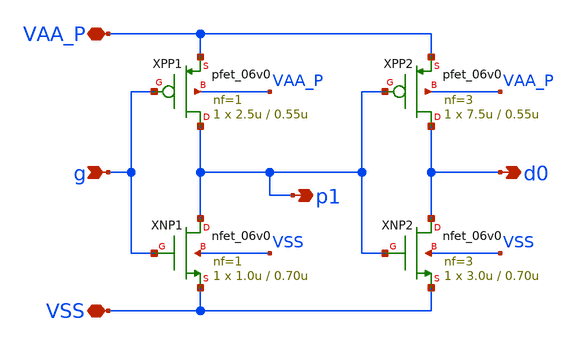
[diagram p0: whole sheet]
** sch_path: xschem/ck_p.sch
**.subckt ck_p g VAA_P d0 p1 VSS
*.ipin g
*.iopin VAA_P
*.opin d0
*.opin p1
*.iopin VSS
XPP1 p1 g VAA_P VAA_P pfet_06v0 L=0.55u W=2.5u nf=1 ad='int((nf+1)/2) * W/nf * 0.18u' as='int((nf+2)/2) * W/nf * 0.18u'
+ pd='2*int((nf+1)/2) * (W/nf + 0.18u)' ps='2*int((nf+2)/2) * (W/nf + 0.18u)' nrd='0.18u / W' nrs='0.18u / W'
+ sa=0 sb=0 sd=0 m=1
XPP2 d0 p1 VAA_P VAA_P pfet_06v0 L=0.55u W=7.5u nf=3 ad='int((nf+1)/2) * W/nf * 0.18u' as='int((nf+2)/2) * W/nf * 0.18u'
+ pd='2*int((nf+1)/2) * (W/nf + 0.18u)' ps='2*int((nf+2)/2) * (W/nf + 0.18u)' nrd='0.18u / W' nrs='0.18u / W'
+ sa=0 sb=0 sd=0 m=1
XNP1 p1 g VSS VSS nfet_06v0 L=0.70u W=1.0u nf=1 ad='int((nf+1)/2) * W/nf * 0.18u' as='int((nf+2)/2) * W/nf * 0.18u'
+ pd='2*int((nf+1)/2) * (W/nf + 0.18u)' ps='2*int((nf+2)/2) * (W/nf + 0.18u)' nrd='0.18u / W' nrs='0.18u / W'
+ sa=0 sb=0 sd=0 m=1 par=1
XNP2 d0 p1 VSS VSS nfet_06v0 L=0.70u W=3.0u nf=3 ad='int((nf+1)/2) * W/nf * 0.18u' as='int((nf+2)/2) * W/nf * 0.18u'
+ pd='2*int((nf+1)/2) * (W/nf + 0.18u)' ps='2*int((nf+2)/2) * (W/nf + 0.18u)' nrd='0.18u / W' nrs='0.18u / W'
+ sa=0 sb=0 sd=0 m=1 par=1
**.ends
.end
